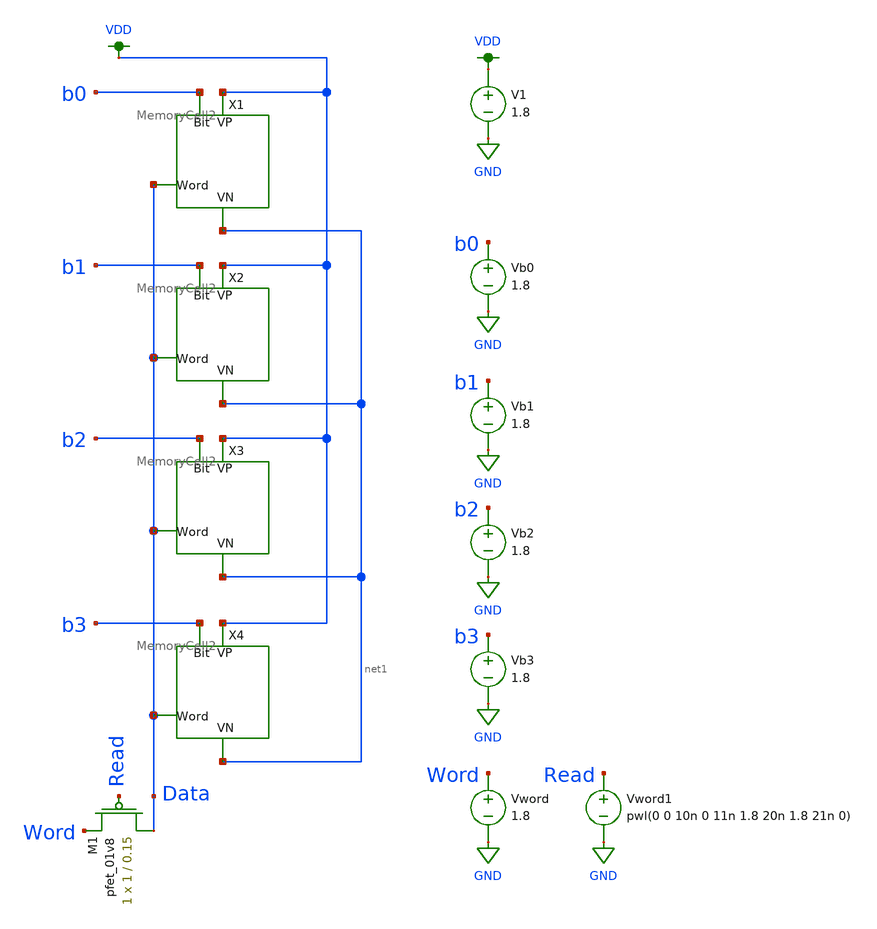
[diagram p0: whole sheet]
** sch_path: DRAM_Components/Schematic/Mem_bin.sch
**.subckt Mem_bin
V1 VDD GND 1.8
Vb0 b0 GND 1.8
Vb1 b1 GND 1.8
Vb2 b2 GND 1.8
Vb3 b3 GND 1.8
Vword Word GND 1.8
Vword1 Read GND pwl(0 0 10n 0 11n 1.8 20n 1.8 21n 0)
XM1 Data Read Word VDD sky130_fd_pr__pfet_01v8 L=0.15 W=1 nf=1 ad='int((nf+1)/2) * W/nf * 0.29' as='int((nf+2)/2) * W/nf * 0.29'
+ pd='2*int((nf+1)/2) * (W/nf + 0.29)' ps='2*int((nf+2)/2) * (W/nf + 0.29)' nrd='0.29 / W' nrs='0.29 / W'
+ sa=0 sb=0 sd=0 mult=1 m=1
X1 VDD net1 Data b0 MemoryCell2
X2 VDD net1 Data b1 MemoryCell2
X3 VDD net1 Data b2 MemoryCell2
X4 VDD net1 Data b3 MemoryCell2
**** begin user architecture code


.control
  set wr_vecnames
  set wr_singlescale
  let code = 0
  while code < 128
    if code eq 0
      let b0 = 0
    else
      let b0 = code % 2
    end
    if floor(code / 2) eq 0
      let b1 = 0
    else
      let b1 = floor(code / 2) % 2
    end
    if floor(code / 4) eq 0
      let b2 = 0
    else
      let b2 = floor(code / 4) % 2
    end
    if floor(code / 8) eq 0
      let b3 = 0
    else
      let b3 = floor(code / 8) % 2
    end

    alter vb0 $&b0
    alter vb1 $&b1
    alter vb2 $&b2
    alter vb3 $&b3
    save all
    op
    wrdata ~/Desktop/ReadWriteTest.txt v(b0) v(b1) v(b2) v(b3) v(Vout)
    if code eq 0
      set appendwrite
      set wr_vecnames = FALSE
    end
    let code = code + 1
  end
  quit
.endc

**** end user architecture code
**.ends

* expanding   symbol:  /home/madvlsi/Desktop/CMOSDRAM/DRAM_Components/Schematic/MemoryCell2.sym # of
*+ pins=4
** sym_path: DRAM_Components/Schematic/MemoryCell2.sym
** sch_path: DRAM_Components/Schematic/MemoryCell2.sch
.subckt MemoryCell2 VP VN Word Bit
*.ipin Bit
*.iopin VP
*.iopin Word
*.iopin VN
XM1 net1 Word Bit VN sky130_fd_pr__nfet_01v8 L=0.15 W=1.05 nf=1 ad='int((nf+1)/2) * W/nf * 0.29' as='int((nf+2)/2) * W/nf * 0.29'
+ pd='2*int((nf+1)/2) * (W/nf + 0.29)' ps='2*int((nf+2)/2) * (W/nf + 0.29)' nrd='0.29 / W' nrs='0.29 / W'
+ sa=0 sb=0 sd=0 mult=1 m=1
XM2 net1 VP net2 VN sky130_fd_pr__nfet_01v8 L=1.6 W=2.0 nf=1 ad='int((nf+1)/2) * W/nf * 0.29' as='int((nf+2)/2) * W/nf * 0.29'
+ pd='2*int((nf+1)/2) * (W/nf + 0.29)' ps='2*int((nf+2)/2) * (W/nf + 0.29)' nrd='0.29 / W' nrs='0.29 / W'
+ sa=0 sb=0 sd=0 mult=1 m=1
XM3 net2 VP net3 VN sky130_fd_pr__nfet_01v8 L=2.0 W=1.13 nf=1 ad='int((nf+1)/2) * W/nf * 0.29' as='int((nf+2)/2) * W/nf * 0.29'
+ pd='2*int((nf+1)/2) * (W/nf + 0.29)' ps='2*int((nf+2)/2) * (W/nf + 0.29)' nrd='0.29 / W' nrs='0.29 / W'
+ sa=0 sb=0 sd=0 mult=1 m=1
XM4 net3 VP net4 VN sky130_fd_pr__nfet_01v8 L=2.35 W=1.11 nf=1 ad='int((nf+1)/2) * W/nf * 0.29' as='int((nf+2)/2) * W/nf * 0.29'
+ pd='2*int((nf+1)/2) * (W/nf + 0.29)' ps='2*int((nf+2)/2) * (W/nf + 0.29)' nrd='0.29 / W' nrs='0.29 / W'
+ sa=0 sb=0 sd=0 mult=1 m=1
XM5 net3 VP net1 VN sky130_fd_pr__nfet_01v8 L=0.65 W=0.95 nf=1 ad='int((nf+1)/2) * W/nf * 0.29' as='int((nf+2)/2) * W/nf * 0.29'
+ pd='2*int((nf+1)/2) * (W/nf + 0.29)' ps='2*int((nf+2)/2) * (W/nf + 0.29)' nrd='0.29 / W' nrs='0.29 / W'
+ sa=0 sb=0 sd=0 mult=1 m=1
C1 net4 VN 1f m=1
.ends

.GLOBAL VDD
.GLOBAL GND
.end
